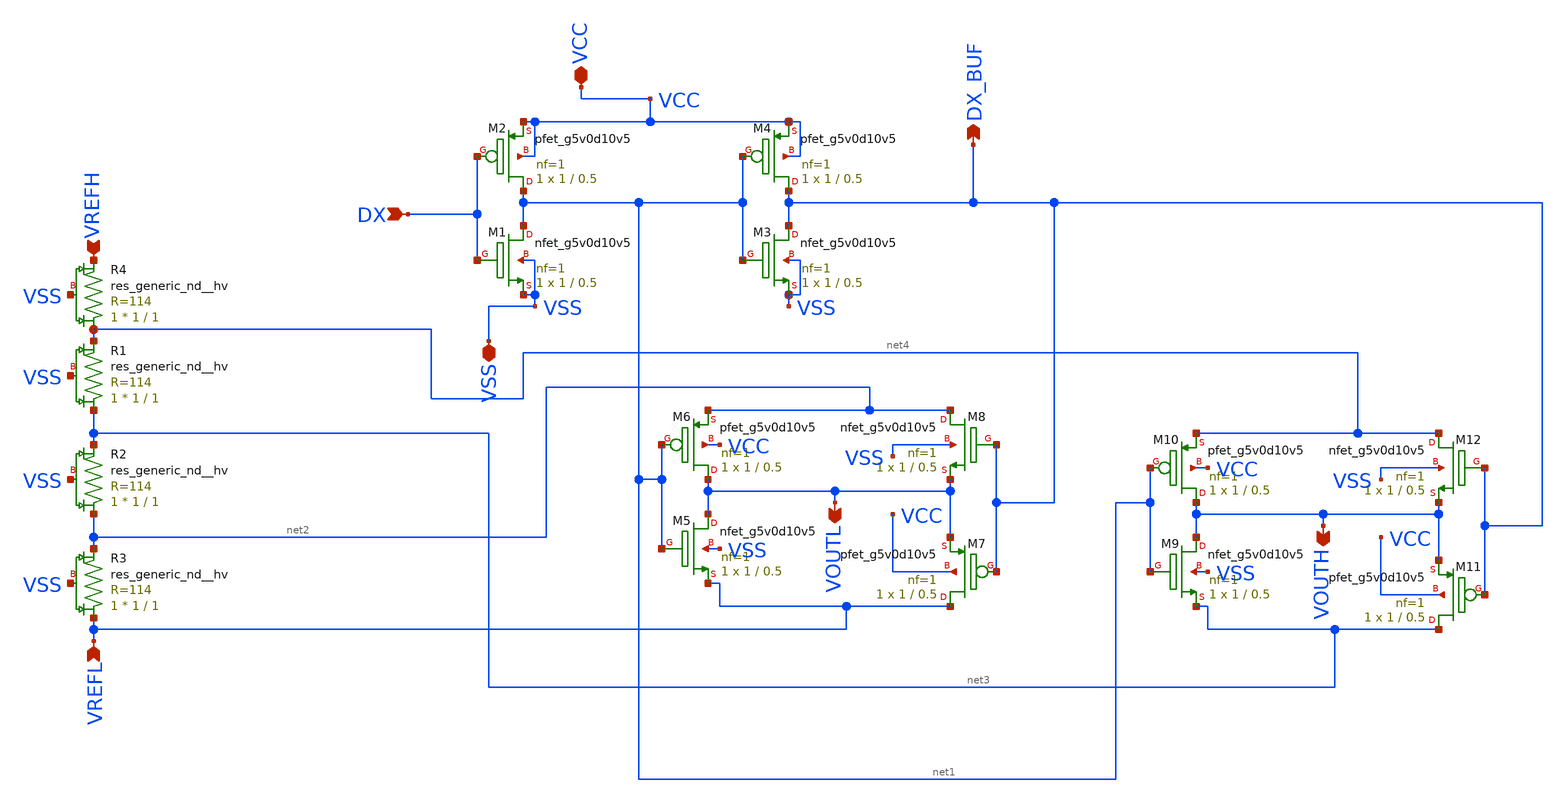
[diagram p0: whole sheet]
** sch_path: Layout_v2/lvs/All_schematic/switch2n_3v3.sch
**.subckt switch2n_3v3 VCC VSS VOUTL DX VOUTH DX_BUF VREFH VREFL
*.iopin VCC
*.iopin VSS
*.opin VOUTL
*.ipin DX
*.opin VOUTH
*.opin DX_BUF
*.ipin VREFH
*.ipin VREFL
XM1 net1 DX VSS VSS sky130_fd_pr__nfet_g5v0d10v5 L=0.5 W=1 nf=1 ad='int((nf+1)/2) * W/nf * 0.29' as='int((nf+2)/2) * W/nf * 0.29'
+ pd='2*int((nf+1)/2) * (W/nf + 0.29)' ps='2*int((nf+2)/2) * (W/nf + 0.29)' nrd='0.29 / W' nrs='0.29 / W'
+ sa=0 sb=0 sd=0 mult=1 m=1
XM2 net1 DX VCC VCC sky130_fd_pr__pfet_g5v0d10v5 L=0.5 W=1 nf=1 ad='int((nf+1)/2) * W/nf * 0.29' as='int((nf+2)/2) * W/nf * 0.29'
+ pd='2*int((nf+1)/2) * (W/nf + 0.29)' ps='2*int((nf+2)/2) * (W/nf + 0.29)' nrd='0.29 / W' nrs='0.29 / W'
+ sa=0 sb=0 sd=0 mult=1 m=1
XM3 DX_BUF net1 VSS VSS sky130_fd_pr__nfet_g5v0d10v5 L=0.5 W=1 nf=1 ad='int((nf+1)/2) * W/nf * 0.29'
+ as='int((nf+2)/2) * W/nf * 0.29' pd='2*int((nf+1)/2) * (W/nf + 0.29)' ps='2*int((nf+2)/2) * (W/nf + 0.29)'
+ nrd='0.29 / W' nrs='0.29 / W' sa=0 sb=0 sd=0 mult=1 m=1
XM4 DX_BUF net1 VCC VCC sky130_fd_pr__pfet_g5v0d10v5 L=0.5 W=1 nf=1 ad='int((nf+1)/2) * W/nf * 0.29'
+ as='int((nf+2)/2) * W/nf * 0.29' pd='2*int((nf+1)/2) * (W/nf + 0.29)' ps='2*int((nf+2)/2) * (W/nf + 0.29)'
+ nrd='0.29 / W' nrs='0.29 / W' sa=0 sb=0 sd=0 mult=1 m=1
XM5 VOUTL net1 VREFL VSS sky130_fd_pr__nfet_g5v0d10v5 L=0.5 W=1 nf=1 ad='int((nf+1)/2) * W/nf * 0.29'
+ as='int((nf+2)/2) * W/nf * 0.29' pd='2*int((nf+1)/2) * (W/nf + 0.29)' ps='2*int((nf+2)/2) * (W/nf + 0.29)'
+ nrd='0.29 / W' nrs='0.29 / W' sa=0 sb=0 sd=0 mult=1 m=1
XM6 VOUTL net1 net2 VCC sky130_fd_pr__pfet_g5v0d10v5 L=0.5 W=1 nf=1 ad='int((nf+1)/2) * W/nf * 0.29'
+ as='int((nf+2)/2) * W/nf * 0.29' pd='2*int((nf+1)/2) * (W/nf + 0.29)' ps='2*int((nf+2)/2) * (W/nf + 0.29)'
+ nrd='0.29 / W' nrs='0.29 / W' sa=0 sb=0 sd=0 mult=1 m=1
XM7 VREFL DX_BUF VOUTL VCC sky130_fd_pr__pfet_g5v0d10v5 L=0.5 W=1 nf=1 ad='int((nf+1)/2) * W/nf * 0.29'
+ as='int((nf+2)/2) * W/nf * 0.29' pd='2*int((nf+1)/2) * (W/nf + 0.29)' ps='2*int((nf+2)/2) * (W/nf + 0.29)'
+ nrd='0.29 / W' nrs='0.29 / W' sa=0 sb=0 sd=0 mult=1 m=1
XM8 net2 DX_BUF VOUTL VSS sky130_fd_pr__nfet_g5v0d10v5 L=0.5 W=1 nf=1 ad='int((nf+1)/2) * W/nf * 0.29'
+ as='int((nf+2)/2) * W/nf * 0.29' pd='2*int((nf+1)/2) * (W/nf + 0.29)' ps='2*int((nf+2)/2) * (W/nf + 0.29)'
+ nrd='0.29 / W' nrs='0.29 / W' sa=0 sb=0 sd=0 mult=1 m=1
XM9 VOUTH net1 net3 VSS sky130_fd_pr__nfet_g5v0d10v5 L=0.5 W=1 nf=1 ad='int((nf+1)/2) * W/nf * 0.29'
+ as='int((nf+2)/2) * W/nf * 0.29' pd='2*int((nf+1)/2) * (W/nf + 0.29)' ps='2*int((nf+2)/2) * (W/nf + 0.29)'
+ nrd='0.29 / W' nrs='0.29 / W' sa=0 sb=0 sd=0 mult=1 m=1
XM10 VOUTH net1 net4 VCC sky130_fd_pr__pfet_g5v0d10v5 L=0.5 W=1 nf=1 ad='int((nf+1)/2) * W/nf * 0.29'
+ as='int((nf+2)/2) * W/nf * 0.29' pd='2*int((nf+1)/2) * (W/nf + 0.29)' ps='2*int((nf+2)/2) * (W/nf + 0.29)'
+ nrd='0.29 / W' nrs='0.29 / W' sa=0 sb=0 sd=0 mult=1 m=1
XM11 net3 DX_BUF VOUTH VCC sky130_fd_pr__pfet_g5v0d10v5 L=0.5 W=1 nf=1 ad='int((nf+1)/2) * W/nf * 0.29'
+ as='int((nf+2)/2) * W/nf * 0.29' pd='2*int((nf+1)/2) * (W/nf + 0.29)' ps='2*int((nf+2)/2) * (W/nf + 0.29)'
+ nrd='0.29 / W' nrs='0.29 / W' sa=0 sb=0 sd=0 mult=1 m=1
XM12 net4 DX_BUF VOUTH VSS sky130_fd_pr__nfet_g5v0d10v5 L=0.5 W=1 nf=1 ad='int((nf+1)/2) * W/nf * 0.29'
+ as='int((nf+2)/2) * W/nf * 0.29' pd='2*int((nf+1)/2) * (W/nf + 0.29)' ps='2*int((nf+2)/2) * (W/nf + 0.29)'
+ nrd='0.29 / W' nrs='0.29 / W' sa=0 sb=0 sd=0 mult=1 m=1
XR1 net3 net4 VSS sky130_fd_pr__res_generic_nd__hv W=1 L=1 mult=1 m=1
XR2 net2 net3 VSS sky130_fd_pr__res_generic_nd__hv W=1 L=1 mult=1 m=1
XR3 VREFL net2 VSS sky130_fd_pr__res_generic_nd__hv W=1 L=1 mult=1 m=1
XR4 net4 VREFH VSS sky130_fd_pr__res_generic_nd__hv W=1 L=1 mult=1 m=1
**.ends
.end
